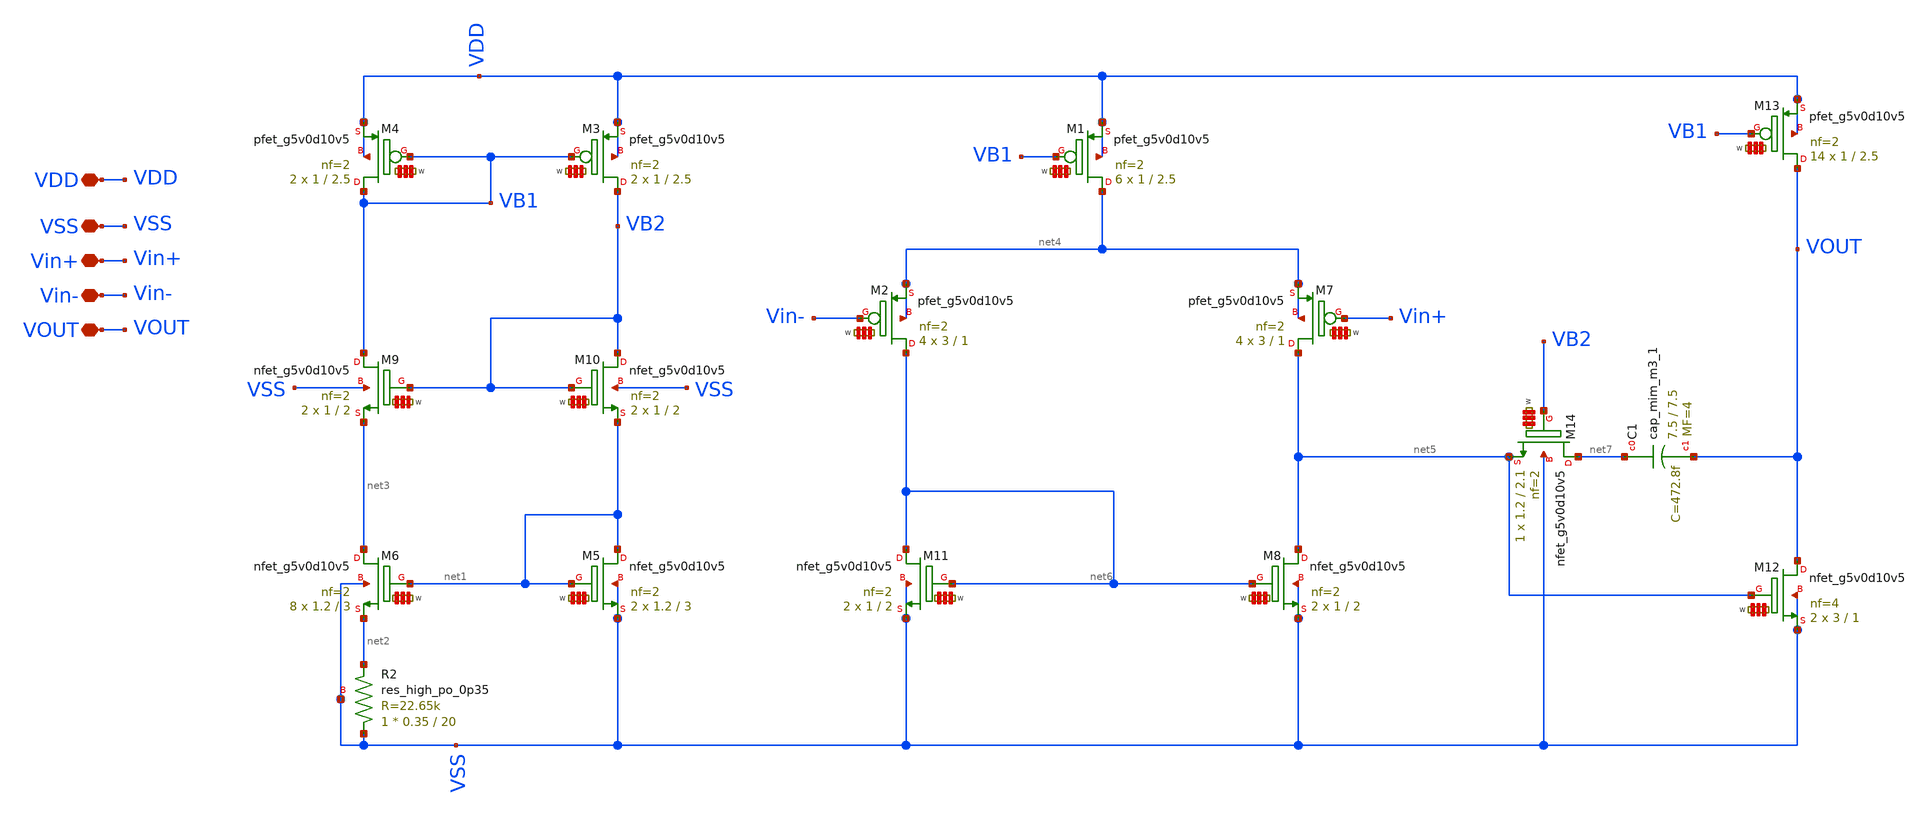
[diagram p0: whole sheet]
** sch_path: my_ip/LIB/Sky130A/Learning/Design_of_Two-Stage_CMOS_Operational_Amplifier_for_Fluorescence_Signal_Processing_5V/A001.sch
**.subckt A001 VDD VSS Vin+ Vin- VOUT
*.iopin VDD
*.iopin VSS
*.iopin Vin+
*.iopin Vin-
*.iopin VOUT
XM9 VB1 VB2 net3 VSS sky130_fd_pr__nfet_g5v0d10v5 L=2 W='1 * 2 ' nf=2 ad='int((nf+1)/2) * W / nf * 0.29'
+ as='int((nf+2)/2) * W / nf * 0.29' pd='2*int((nf+1)/2) * (W / nf + 0.29)' ps='2*int((nf+2)/2) * (W / nf + 0.29)'
+ nrd='0.29 / W ' nrs='0.29 / W ' sa=0 sb=0 sd=0 mult=2 m=2
XM10 VB2 VB2 net1 VSS sky130_fd_pr__nfet_g5v0d10v5 L=2 W='1 * 2 ' nf=2 ad='int((nf+1)/2) * W / nf * 0.29'
+ as='int((nf+2)/2) * W / nf * 0.29' pd='2*int((nf+1)/2) * (W / nf + 0.29)' ps='2*int((nf+2)/2) * (W / nf + 0.29)'
+ nrd='0.29 / W ' nrs='0.29 / W ' sa=0 sb=0 sd=0 mult=2 m=2
XM3 VB2 VB1 VDD VDD sky130_fd_pr__pfet_g5v0d10v5 L=2.5 W='1 * 2 ' nf=2 ad='int((2 + 1)/2) * 1 * 0.29'
+ as='int((2 + 2)/2) * 1 * 0.29' pd='2*int((2 + 1)/2) * (1 + 0.29)' ps='2*int((2 + 2)/2) * (1 + 0.29)'
+ nrd='0.29 / 1 / 2 ' nrs='0.29 / 1 / 2 ' sa=0 sb=0 sd=0 mult=2 m=2
XM4 VB1 VB1 VDD VDD sky130_fd_pr__pfet_g5v0d10v5 L=2.5 W='1 * 2 ' nf=2 ad='int((2 + 1)/2) * 1 * 0.29'
+ as='int((2 + 2)/2) * 1 * 0.29' pd='2*int((2 + 1)/2) * (1 + 0.29)' ps='2*int((2 + 2)/2) * (1 + 0.29)'
+ nrd='0.29 / 1 / 2 ' nrs='0.29 / 1 / 2 ' sa=0 sb=0 sd=0 mult=2 m=2
XM5 net1 net1 VSS VSS sky130_fd_pr__nfet_g5v0d10v5 L=3 W='1.2 * 2 ' nf=2 ad='int((nf+1)/2) * W / nf * 0.29'
+ as='int((nf+2)/2) * W / nf * 0.29' pd='2*int((nf+1)/2) * (W / nf + 0.29)' ps='2*int((nf+2)/2) * (W / nf + 0.29)'
+ nrd='0.29 / W ' nrs='0.29 / W ' sa=0 sb=0 sd=0 mult=2 m=2
XM6 net3 net1 net2 VSS sky130_fd_pr__nfet_g5v0d10v5 L=3 W='1.2 * 2 ' nf=2 ad='int((nf+1)/2) * W / nf * 0.29'
+ as='int((nf+2)/2) * W / nf * 0.29' pd='2*int((nf+1)/2) * (W / nf + 0.29)' ps='2*int((nf+2)/2) * (W / nf + 0.29)'
+ nrd='0.29 / W ' nrs='0.29 / W ' sa=0 sb=0 sd=0 mult=8 m=8
XR2 VSS net2 VSS sky130_fd_pr__res_high_po_0p35 L=20 mult=1 m=1
XM1 net4 VB1 VDD VDD sky130_fd_pr__pfet_g5v0d10v5 L=2.5 W='1 * 2 ' nf=2 ad='int((2 + 1)/2) * 1 * 0.29'
+ as='int((2 + 2)/2) * 1 * 0.29' pd='2*int((2 + 1)/2) * (1 + 0.29)' ps='2*int((2 + 2)/2) * (1 + 0.29)'
+ nrd='0.29 / 1 / 2 ' nrs='0.29 / 1 / 2 ' sa=0 sb=0 sd=0 mult=6 m=6
XM2 net6 Vin- net4 net4 sky130_fd_pr__pfet_g5v0d10v5 L=1 W='3 * 2 ' nf=2 ad='int((2 + 1)/2) * 3 * 0.29'
+ as='int((2 + 2)/2) * 3 * 0.29' pd='2*int((2 + 1)/2) * (3 + 0.29)' ps='2*int((2 + 2)/2) * (3 + 0.29)'
+ nrd='0.29 / 3 / 2 ' nrs='0.29 / 3 / 2 ' sa=0 sb=0 sd=0 mult=4 m=4
XM11 net6 net6 VSS VSS sky130_fd_pr__nfet_g5v0d10v5 L=2 W='1 * 2 ' nf=2 ad='int((nf+1)/2) * W / nf * 0.29'
+ as='int((nf+2)/2) * W / nf * 0.29' pd='2*int((nf+1)/2) * (W / nf + 0.29)' ps='2*int((nf+2)/2) * (W / nf + 0.29)'
+ nrd='0.29 / W ' nrs='0.29 / W ' sa=0 sb=0 sd=0 mult=2 m=2
XM8 net5 net6 VSS VSS sky130_fd_pr__nfet_g5v0d10v5 L=2 W='1 * 2 ' nf=2 ad='int((nf+1)/2) * W / nf * 0.29'
+ as='int((nf+2)/2) * W / nf * 0.29' pd='2*int((nf+1)/2) * (W / nf + 0.29)' ps='2*int((nf+2)/2) * (W / nf + 0.29)'
+ nrd='0.29 / W ' nrs='0.29 / W ' sa=0 sb=0 sd=0 mult=2 m=2
XM12 VOUT net5 VSS VSS sky130_fd_pr__nfet_g5v0d10v5 L=1 W='3 * 4 ' nf=4 ad='int((nf+1)/2) * W / nf * 0.29'
+ as='int((nf+2)/2) * W / nf * 0.29' pd='2*int((nf+1)/2) * (W / nf + 0.29)' ps='2*int((nf+2)/2) * (W / nf + 0.29)'
+ nrd='0.29 / W ' nrs='0.29 / W ' sa=0 sb=0 sd=0 mult=2 m=2
XM7 net5 Vin+ net4 net4 sky130_fd_pr__pfet_g5v0d10v5 L=1 W='3 * 2 ' nf=2 ad='int((2 + 1)/2) * 3 * 0.29'
+ as='int((2 + 2)/2) * 3 * 0.29' pd='2*int((2 + 1)/2) * (3 + 0.29)' ps='2*int((2 + 2)/2) * (3 + 0.29)'
+ nrd='0.29 / 3 / 2 ' nrs='0.29 / 3 / 2 ' sa=0 sb=0 sd=0 mult=4 m=4
XM13 VOUT VB1 VDD VDD sky130_fd_pr__pfet_g5v0d10v5 L=2.5 W='1 * 2 ' nf=2 ad='int((2 + 1)/2) * 1 * 0.29'
+ as='int((2 + 2)/2) * 1 * 0.29' pd='2*int((2 + 1)/2) * (1 + 0.29)' ps='2*int((2 + 2)/2) * (1 + 0.29)'
+ nrd='0.29 / 1 / 2 ' nrs='0.29 / 1 / 2 ' sa=0 sb=0 sd=0 mult=14 m=14
XM14 net7 VB2 net5 VSS sky130_fd_pr__nfet_g5v0d10v5 L=2.1 W='1.2 * 2 ' nf=2 ad='int((nf+1)/2) * W / nf * 0.29'
+ as='int((nf+2)/2) * W / nf * 0.29' pd='2*int((nf+1)/2) * (W / nf + 0.29)' ps='2*int((nf+2)/2) * (W / nf + 0.29)'
+ nrd='0.29 / W ' nrs='0.29 / W ' sa=0 sb=0 sd=0 mult=1 m=1
XC1 net7 VOUT sky130_fd_pr__cap_mim_m3_1 W=7.5 L=7.5 MF=4 m=4
**.ends
.end
